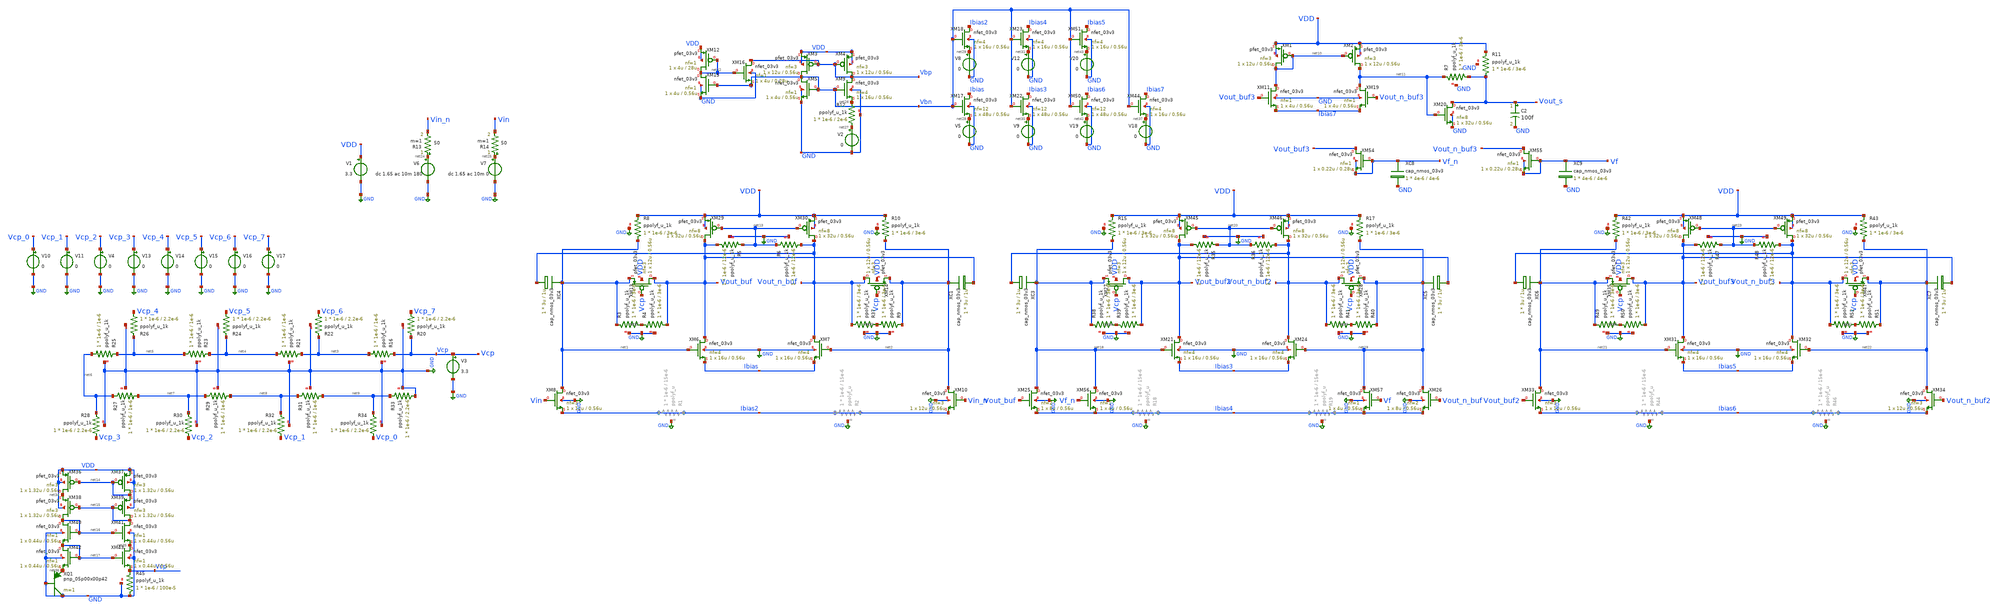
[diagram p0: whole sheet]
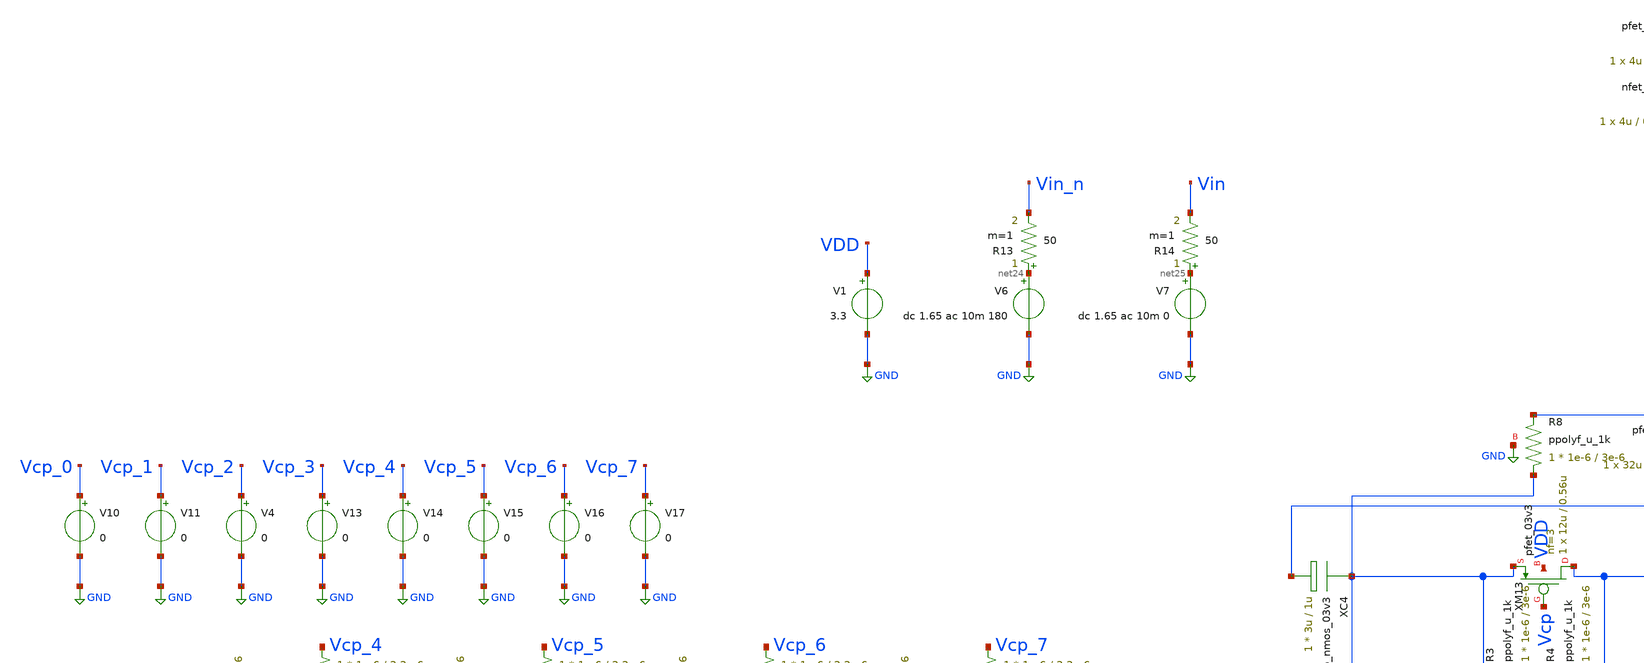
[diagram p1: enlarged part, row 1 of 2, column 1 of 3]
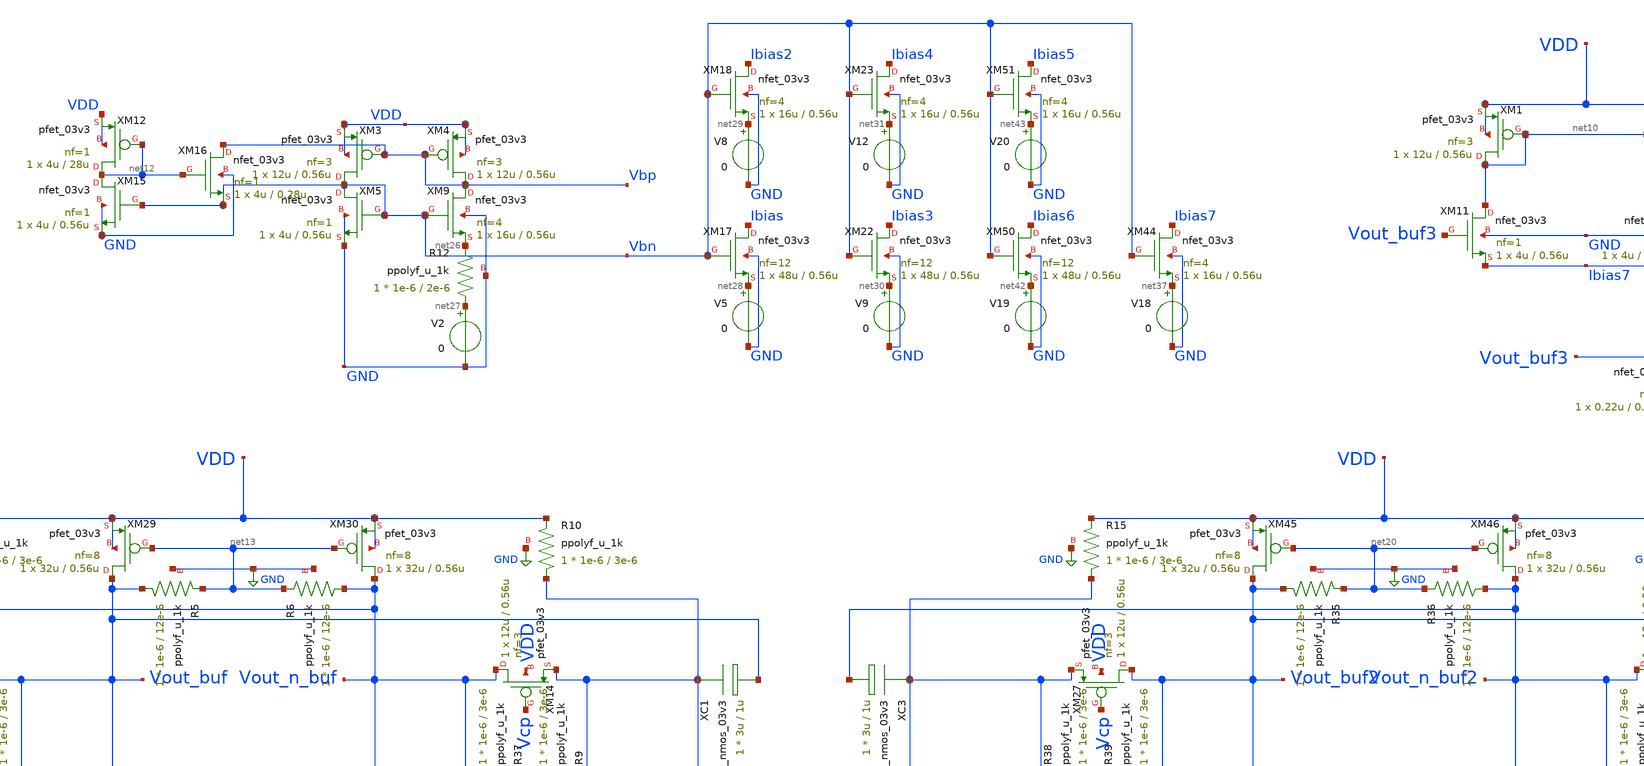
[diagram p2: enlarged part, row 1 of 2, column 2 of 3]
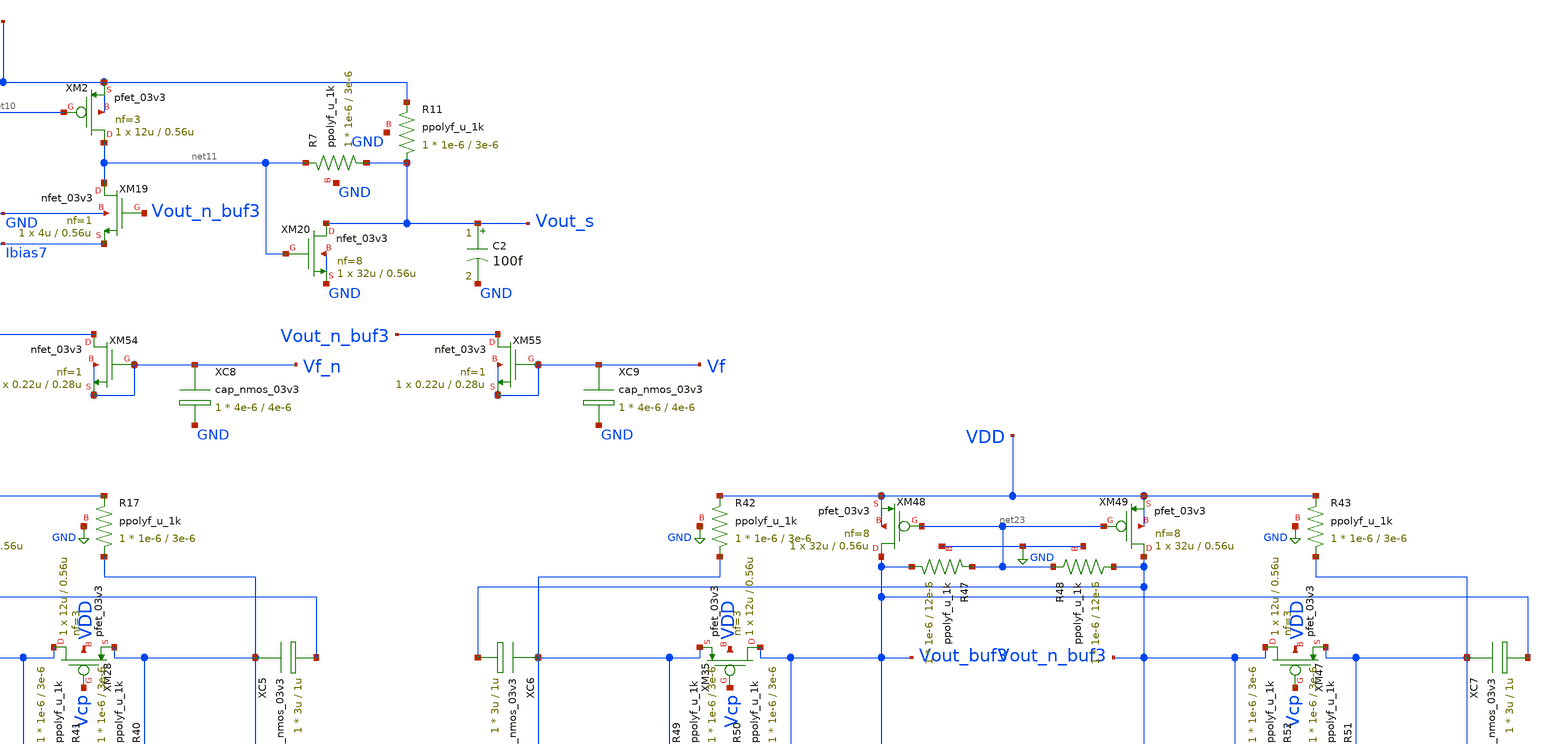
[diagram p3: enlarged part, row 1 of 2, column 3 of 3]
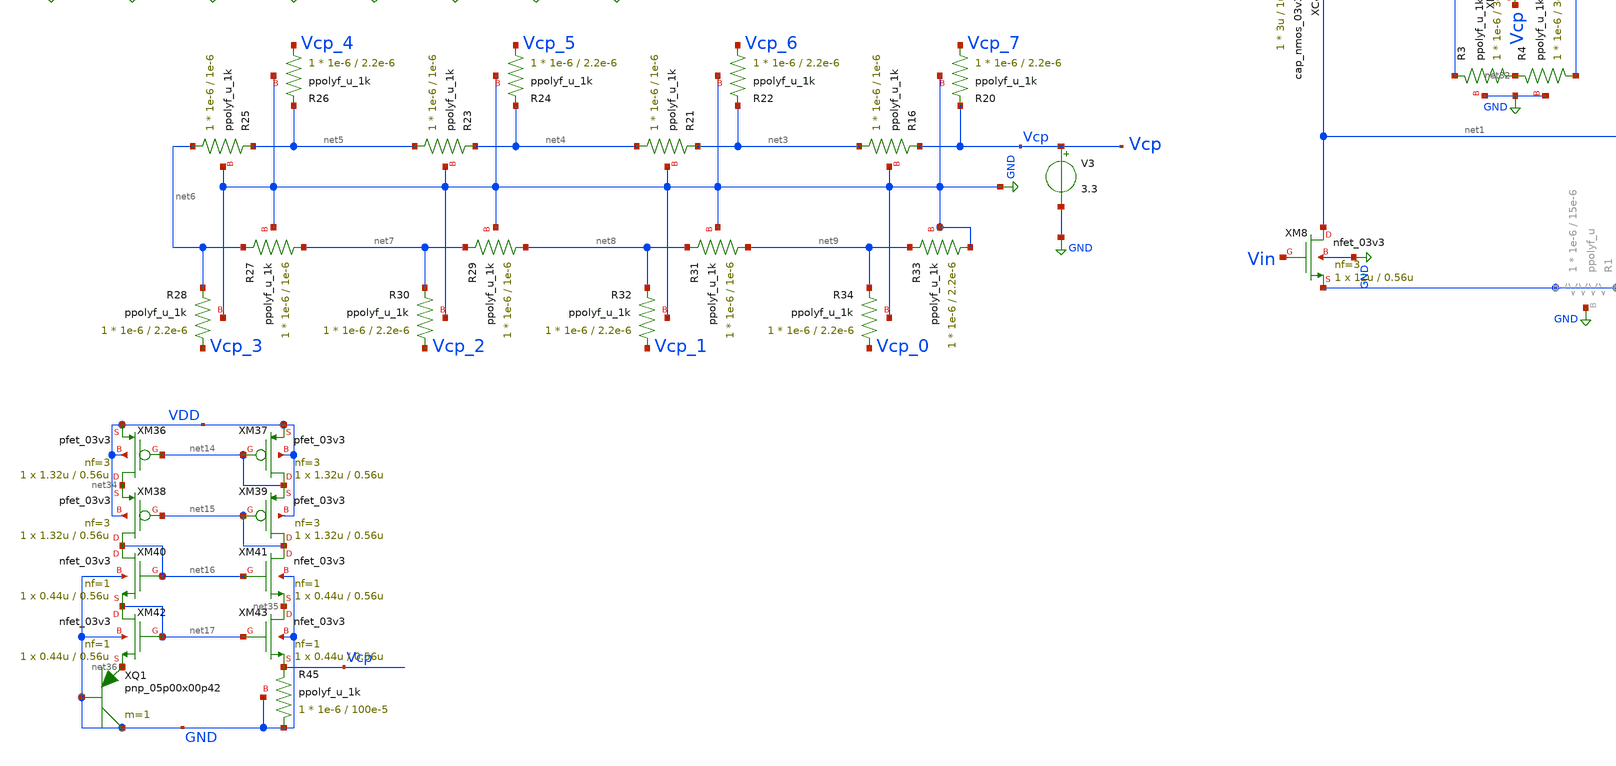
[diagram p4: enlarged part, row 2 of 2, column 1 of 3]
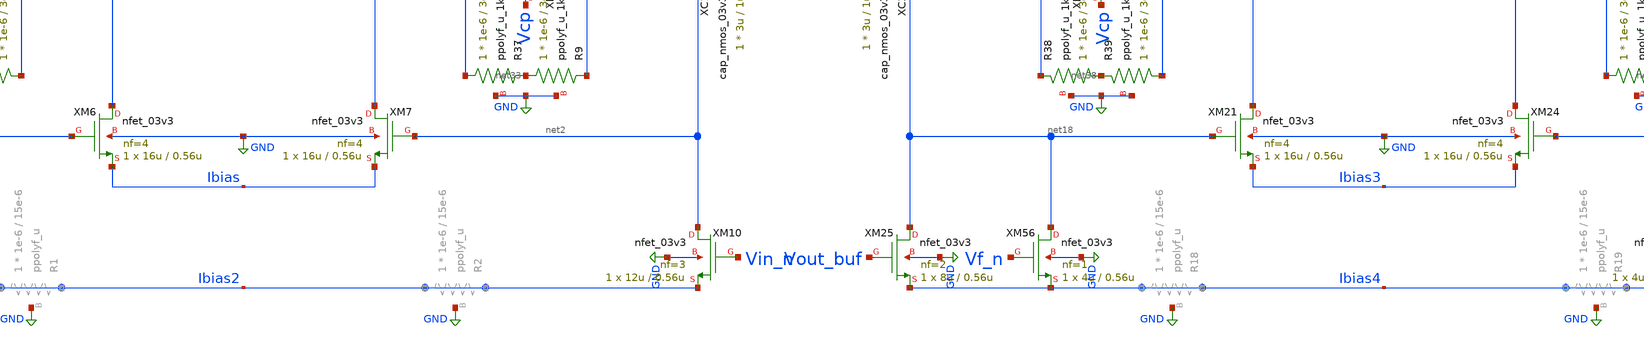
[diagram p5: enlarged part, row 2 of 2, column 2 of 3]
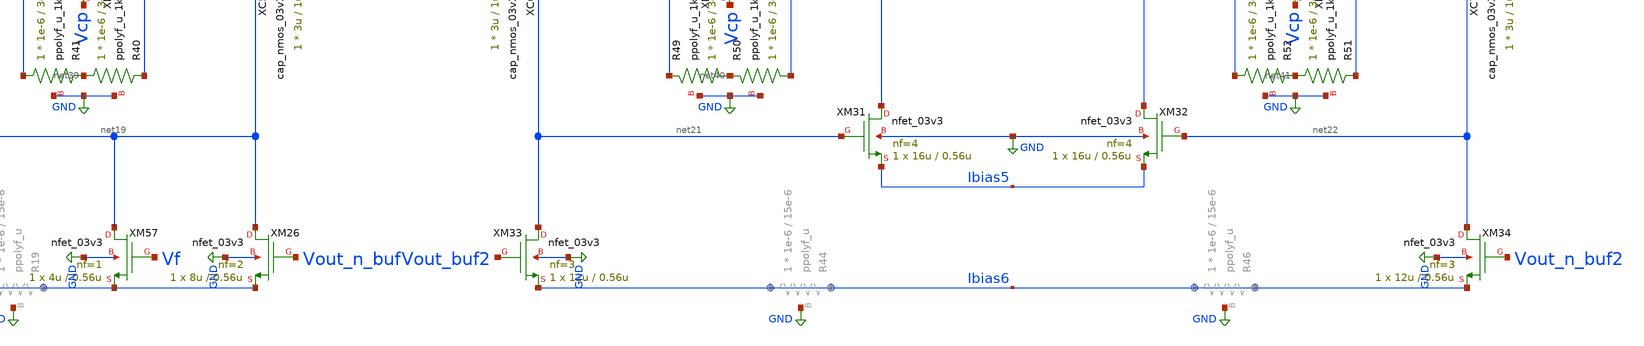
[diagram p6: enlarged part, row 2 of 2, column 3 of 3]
** sch_path: blocks/vga/vga.sch
**.subckt vga
V1 VDD GND 3.3
V6 net24 GND dc 1.65 ac 10m 180
XM6 Vout_buf net1 Ibias GND nfet_03v3 L=0.56u W=16u nf=4 ad='int((nf+1)/2) * W/nf * 0.18u' as='int((nf+2)/2) * W/nf * 0.18u'
+ pd='2*int((nf+1)/2) * (W/nf + 0.18u)' ps='2*int((nf+2)/2) * (W/nf + 0.18u)' nrd='0.18u / W' nrs='0.18u / W'
+ sa=0 sb=0 sd=0 m=1
XM7 Vout_n_buf net2 Ibias GND nfet_03v3 L=0.56u W=16u nf=4 ad='int((nf+1)/2) * W/nf * 0.18u' as='int((nf+2)/2) * W/nf * 0.18u'
+ pd='2*int((nf+1)/2) * (W/nf + 0.18u)' ps='2*int((nf+2)/2) * (W/nf + 0.18u)' nrd='0.18u / W' nrs='0.18u / W'
+ sa=0 sb=0 sd=0 m=1
XM8 net1 Vin Ibias2 GND nfet_03v3 L=0.56u W=12u nf=3 ad='int((nf+1)/2) * W/nf * 0.18u' as='int((nf+2)/2) * W/nf * 0.18u'
+ pd='2*int((nf+1)/2) * (W/nf + 0.18u)' ps='2*int((nf+2)/2) * (W/nf + 0.18u)' nrd='0.18u / W' nrs='0.18u / W'
+ sa=0 sb=0 sd=0 m=1
XM10 net2 Vin_n Ibias2 GND nfet_03v3 L=0.56u W=12u nf=3 ad='int((nf+1)/2) * W/nf * 0.18u' as='int((nf+2)/2) * W/nf * 0.18u'
+ pd='2*int((nf+1)/2) * (W/nf + 0.18u)' ps='2*int((nf+2)/2) * (W/nf + 0.18u)' nrd='0.18u / W' nrs='0.18u / W'
+ sa=0 sb=0 sd=0 m=1
V7 net25 GND dc 1.65 ac 10m 0
R14 net25 Vin 50 m=1
R13 net24 Vin_n 50 m=1
XR16 net3 Vcp GND ppolyf_u_1k r_width=1e-6 r_length=1e-6 m=1
XR20 Vcp_7 Vcp GND ppolyf_u_1k r_width=1e-6 r_length=2.2e-6 m=1
XR21 net4 net3 GND ppolyf_u_1k r_width=1e-6 r_length=1e-6 m=1
XR22 Vcp_6 net3 GND ppolyf_u_1k r_width=1e-6 r_length=2.2e-6 m=1
XR23 net5 net4 GND ppolyf_u_1k r_width=1e-6 r_length=1e-6 m=1
XR24 Vcp_5 net4 GND ppolyf_u_1k r_width=1e-6 r_length=2.2e-6 m=1
XR25 net6 net5 GND ppolyf_u_1k r_width=1e-6 r_length=1e-6 m=1
XR26 Vcp_4 net5 GND ppolyf_u_1k r_width=1e-6 r_length=2.2e-6 m=1
XR27 net7 net6 GND ppolyf_u_1k r_width=1e-6 r_length=1e-6 m=1
XR28 Vcp_3 net6 GND ppolyf_u_1k r_width=1e-6 r_length=2.2e-6 m=1
XR29 net8 net7 GND ppolyf_u_1k r_width=1e-6 r_length=1e-6 m=1
XR30 Vcp_2 net7 GND ppolyf_u_1k r_width=1e-6 r_length=2.2e-6 m=1
XR31 net9 net8 GND ppolyf_u_1k r_width=1e-6 r_length=1e-6 m=1
XR32 Vcp_1 net8 GND ppolyf_u_1k r_width=1e-6 r_length=2.2e-6 m=1
XR33 GND net9 GND ppolyf_u_1k r_width=1e-6 r_length=2.2e-6 m=1
XR34 Vcp_0 net9 GND ppolyf_u_1k r_width=1e-6 r_length=2.2e-6 m=1
V10 Vcp_0 GND 0
V11 Vcp_1 GND 0
V4 Vcp_2 GND 0
V13 Vcp_3 GND 0
V14 Vcp_4 GND 0
V15 Vcp_5 GND 0
V16 Vcp_6 GND 0
V17 Vcp_7 GND 0
V3 Vcp GND 3.3
XM13 Vout_buf Vcp net1 VDD pfet_03v3 L=0.56u W=12u nf=3 ad='int((nf+1)/2) * W/nf * 0.18u' as='int((nf+2)/2) * W/nf * 0.18u'
+ pd='2*int((nf+1)/2) * (W/nf + 0.18u)' ps='2*int((nf+2)/2) * (W/nf + 0.18u)' nrd='0.18u / W' nrs='0.18u / W'
+ sa=0 sb=0 sd=0 m=1
XM14 Vout_n_buf Vcp net2 VDD pfet_03v3 L=0.56u W=12u nf=3 ad='int((nf+1)/2) * W/nf * 0.18u' as='int((nf+2)/2) * W/nf * 0.18u'
+ pd='2*int((nf+1)/2) * (W/nf + 0.18u)' ps='2*int((nf+2)/2) * (W/nf + 0.18u)' nrd='0.18u / W' nrs='0.18u / W'
+ sa=0 sb=0 sd=0 m=1
XR8 net1 VDD GND ppolyf_u_1k r_width=1e-6 r_length=3e-6 m=1
XR10 net2 VDD GND ppolyf_u_1k r_width=1e-6 r_length=3e-6 m=1
XC4 net1 Vout_n_buf cap_nmos_03v3 c_width=3u c_length=1u m=1
XC1 net2 Vout_buf cap_nmos_03v3 c_width=3u c_length=1u m=1
XM11 net10 Vout_buf3 Ibias7 GND nfet_03v3 L=0.56u W=4u nf=1 ad='int((nf+1)/2) * W/nf * 0.18u' as='int((nf+2)/2) * W/nf * 0.18u'
+ pd='2*int((nf+1)/2) * (W/nf + 0.18u)' ps='2*int((nf+2)/2) * (W/nf + 0.18u)' nrd='0.18u / W' nrs='0.18u / W'
+ sa=0 sb=0 sd=0 m=1
XM19 net11 Vout_n_buf3 Ibias7 GND nfet_03v3 L=0.56u W=4u nf=1 ad='int((nf+1)/2) * W/nf * 0.18u' as='int((nf+2)/2) * W/nf * 0.18u'
+ pd='2*int((nf+1)/2) * (W/nf + 0.18u)' ps='2*int((nf+2)/2) * (W/nf + 0.18u)' nrd='0.18u / W' nrs='0.18u / W'
+ sa=0 sb=0 sd=0 m=1
XR7 Vout_s net11 GND ppolyf_u_1k r_width=1e-6 r_length=3e-6 m=1
XM20 Vout_s net11 GND GND nfet_03v3 L=0.56u W=32u nf=8 ad='int((nf+1)/2) * W/nf * 0.18u' as='int((nf+2)/2) * W/nf * 0.18u'
+ pd='2*int((nf+1)/2) * (W/nf + 0.18u)' ps='2*int((nf+2)/2) * (W/nf + 0.18u)' nrd='0.18u / W' nrs='0.18u / W'
+ sa=0 sb=0 sd=0 m=1
C2 Vout_s GND 100f m=1
XR11 Vout_s VDD GND ppolyf_u_1k r_width=1e-6 r_length=3e-6 m=1
XM1 net10 net10 VDD VDD pfet_03v3 L=0.56u W=12u nf=3 ad='int((nf+1)/2) * W/nf * 0.18u' as='int((nf+2)/2) * W/nf * 0.18u'
+ pd='2*int((nf+1)/2) * (W/nf + 0.18u)' ps='2*int((nf+2)/2) * (W/nf + 0.18u)' nrd='0.18u / W' nrs='0.18u / W'
+ sa=0 sb=0 sd=0 m=1
XM2 net11 net10 VDD VDD pfet_03v3 L=0.56u W=12u nf=3 ad='int((nf+1)/2) * W/nf * 0.18u' as='int((nf+2)/2) * W/nf * 0.18u'
+ pd='2*int((nf+1)/2) * (W/nf + 0.18u)' ps='2*int((nf+2)/2) * (W/nf + 0.18u)' nrd='0.18u / W' nrs='0.18u / W'
+ sa=0 sb=0 sd=0 m=1
XM3 Vbn Vbp VDD VDD pfet_03v3 L=0.56u W=12u nf=3 ad='int((nf+1)/2) * W/nf * 0.18u' as='int((nf+2)/2) * W/nf * 0.18u'
+ pd='2*int((nf+1)/2) * (W/nf + 0.18u)' ps='2*int((nf+2)/2) * (W/nf + 0.18u)' nrd='0.18u / W' nrs='0.18u / W'
+ sa=0 sb=0 sd=0 m=1
XM4 Vbp Vbp VDD VDD pfet_03v3 L=0.56u W=12u nf=3 ad='int((nf+1)/2) * W/nf * 0.18u' as='int((nf+2)/2) * W/nf * 0.18u'
+ pd='2*int((nf+1)/2) * (W/nf + 0.18u)' ps='2*int((nf+2)/2) * (W/nf + 0.18u)' nrd='0.18u / W' nrs='0.18u / W'
+ sa=0 sb=0 sd=0 m=1
XM5 Vbn Vbn GND GND nfet_03v3 L=0.56u W=4u nf=1 ad='int((nf+1)/2) * W/nf * 0.18u' as='int((nf+2)/2) * W/nf * 0.18u'
+ pd='2*int((nf+1)/2) * (W/nf + 0.18u)' ps='2*int((nf+2)/2) * (W/nf + 0.18u)' nrd='0.18u / W' nrs='0.18u / W'
+ sa=0 sb=0 sd=0 m=1
XM9 Vbp Vbn net26 GND nfet_03v3 L=0.56u W=16u nf=4 ad='int((nf+1)/2) * W/nf * 0.18u' as='int((nf+2)/2) * W/nf * 0.18u'
+ pd='2*int((nf+1)/2) * (W/nf + 0.18u)' ps='2*int((nf+2)/2) * (W/nf + 0.18u)' nrd='0.18u / W' nrs='0.18u / W'
+ sa=0 sb=0 sd=0 m=1
XM12 net12 net12 VDD VDD pfet_03v3 L=28u W=4u nf=1 ad='int((nf+1)/2) * W/nf * 0.18u' as='int((nf+2)/2) * W/nf * 0.18u'
+ pd='2*int((nf+1)/2) * (W/nf + 0.18u)' ps='2*int((nf+2)/2) * (W/nf + 0.18u)' nrd='0.18u / W' nrs='0.18u / W'
+ sa=0 sb=0 sd=0 m=1
XM15 net12 Vbn GND GND nfet_03v3 L=0.56u W=4u nf=1 ad='int((nf+1)/2) * W/nf * 0.18u' as='int((nf+2)/2) * W/nf * 0.18u'
+ pd='2*int((nf+1)/2) * (W/nf + 0.18u)' ps='2*int((nf+2)/2) * (W/nf + 0.18u)' nrd='0.18u / W' nrs='0.18u / W'
+ sa=0 sb=0 sd=0 m=1
XM16 Vbp net12 Vbn GND nfet_03v3 L=0.28u W=4u nf=1 ad='int((nf+1)/2) * W/nf * 0.18u' as='int((nf+2)/2) * W/nf * 0.18u'
+ pd='2*int((nf+1)/2) * (W/nf + 0.18u)' ps='2*int((nf+2)/2) * (W/nf + 0.18u)' nrd='0.18u / W' nrs='0.18u / W'
+ sa=0 sb=0 sd=0 m=1
XR12 net27 net26 GND ppolyf_u_1k r_width=1e-6 r_length=2e-6 m=1
V2 net27 GND 0
XM17 Ibias Vbn net28 GND nfet_03v3 L=0.56u W=48u nf=12 ad='int((nf+1)/2) * W/nf * 0.18u' as='int((nf+2)/2) * W/nf * 0.18u'
+ pd='2*int((nf+1)/2) * (W/nf + 0.18u)' ps='2*int((nf+2)/2) * (W/nf + 0.18u)' nrd='0.18u / W' nrs='0.18u / W'
+ sa=0 sb=0 sd=0 m=1
V5 net28 GND 0
XM18 Ibias2 Vbn net29 GND nfet_03v3 L=0.56u W=16u nf=4 ad='int((nf+1)/2) * W/nf * 0.18u' as='int((nf+2)/2) * W/nf * 0.18u'
+ pd='2*int((nf+1)/2) * (W/nf + 0.18u)' ps='2*int((nf+2)/2) * (W/nf + 0.18u)' nrd='0.18u / W' nrs='0.18u / W'
+ sa=0 sb=0 sd=0 m=1
V8 net29 GND 0
XM22 Ibias3 Vbn net30 GND nfet_03v3 L=0.56u W=48u nf=12 ad='int((nf+1)/2) * W/nf * 0.18u' as='int((nf+2)/2) * W/nf * 0.18u'
+ pd='2*int((nf+1)/2) * (W/nf + 0.18u)' ps='2*int((nf+2)/2) * (W/nf + 0.18u)' nrd='0.18u / W' nrs='0.18u / W'
+ sa=0 sb=0 sd=0 m=1
V9 net30 GND 0
XM23 Ibias4 Vbn net31 GND nfet_03v3 L=0.56u W=16u nf=4 ad='int((nf+1)/2) * W/nf * 0.18u' as='int((nf+2)/2) * W/nf * 0.18u'
+ pd='2*int((nf+1)/2) * (W/nf + 0.18u)' ps='2*int((nf+2)/2) * (W/nf + 0.18u)' nrd='0.18u / W' nrs='0.18u / W'
+ sa=0 sb=0 sd=0 m=1
V12 net31 GND 0
XM29 Vout_buf net13 VDD VDD pfet_03v3 L=0.56u W=32u nf=8 ad='int((nf+1)/2) * W/nf * 0.18u' as='int((nf+2)/2) * W/nf * 0.18u'
+ pd='2*int((nf+1)/2) * (W/nf + 0.18u)' ps='2*int((nf+2)/2) * (W/nf + 0.18u)' nrd='0.18u / W' nrs='0.18u / W'
+ sa=0 sb=0 sd=0 m=1
XM30 Vout_n_buf net13 VDD VDD pfet_03v3 L=0.56u W=32u nf=8 ad='int((nf+1)/2) * W/nf * 0.18u' as='int((nf+2)/2) * W/nf * 0.18u'
+ pd='2*int((nf+1)/2) * (W/nf + 0.18u)' ps='2*int((nf+2)/2) * (W/nf + 0.18u)' nrd='0.18u / W' nrs='0.18u / W'
+ sa=0 sb=0 sd=0 m=1
XR5 Vout_buf net13 GND ppolyf_u_1k r_width=1e-6 r_length=12e-6 m=1
XR6 Vout_n_buf net13 GND ppolyf_u_1k r_width=1e-6 r_length=12e-6 m=1
XR3 net32 net1 GND ppolyf_u_1k r_width=1e-6 r_length=3e-6 m=1
XR4 Vout_buf net32 GND ppolyf_u_1k r_width=1e-6 r_length=3e-6 m=1
XR9 net33 net2 GND ppolyf_u_1k r_width=1e-6 r_length=3e-6 m=1
XR37 Vout_n_buf net33 GND ppolyf_u_1k r_width=1e-6 r_length=3e-6 m=1
XM36 net34 net14 VDD VDD pfet_03v3 L=0.56u W=1.32u nf=3 ad='int((nf+1)/2) * W/nf * 0.18u' as='int((nf+2)/2) * W/nf * 0.18u'
+ pd='2*int((nf+1)/2) * (W/nf + 0.18u)' ps='2*int((nf+2)/2) * (W/nf + 0.18u)' nrd='0.18u / W' nrs='0.18u / W'
+ sa=0 sb=0 sd=0 m=1
XM37 net14 net14 VDD VDD pfet_03v3 L=0.56u W=1.32u nf=3 ad='int((nf+1)/2) * W/nf * 0.18u' as='int((nf+2)/2) * W/nf * 0.18u'
+ pd='2*int((nf+1)/2) * (W/nf + 0.18u)' ps='2*int((nf+2)/2) * (W/nf + 0.18u)' nrd='0.18u / W' nrs='0.18u / W'
+ sa=0 sb=0 sd=0 m=1
XM38 net16 net15 net34 VDD pfet_03v3 L=0.56u W=1.32u nf=3 ad='int((nf+1)/2) * W/nf * 0.18u' as='int((nf+2)/2) * W/nf * 0.18u'
+ pd='2*int((nf+1)/2) * (W/nf + 0.18u)' ps='2*int((nf+2)/2) * (W/nf + 0.18u)' nrd='0.18u / W' nrs='0.18u / W'
+ sa=0 sb=0 sd=0 m=1
XM39 net15 net15 net14 VDD pfet_03v3 L=0.56u W=1.32u nf=3 ad='int((nf+1)/2) * W/nf * 0.18u' as='int((nf+2)/2) * W/nf * 0.18u'
+ pd='2*int((nf+1)/2) * (W/nf + 0.18u)' ps='2*int((nf+2)/2) * (W/nf + 0.18u)' nrd='0.18u / W' nrs='0.18u / W'
+ sa=0 sb=0 sd=0 m=1
XM40 net16 net16 net17 GND nfet_03v3 L=0.56u W=0.44u nf=1 ad='int((nf+1)/2) * W/nf * 0.18u' as='int((nf+2)/2) * W/nf * 0.18u'
+ pd='2*int((nf+1)/2) * (W/nf + 0.18u)' ps='2*int((nf+2)/2) * (W/nf + 0.18u)' nrd='0.18u / W' nrs='0.18u / W'
+ sa=0 sb=0 sd=0 m=1
XM41 net15 net16 net35 GND nfet_03v3 L=0.56u W=0.44u nf=1 ad='int((nf+1)/2) * W/nf * 0.18u' as='int((nf+2)/2) * W/nf * 0.18u'
+ pd='2*int((nf+1)/2) * (W/nf + 0.18u)' ps='2*int((nf+2)/2) * (W/nf + 0.18u)' nrd='0.18u / W' nrs='0.18u / W'
+ sa=0 sb=0 sd=0 m=1
XM42 net17 net17 net36 GND nfet_03v3 L=0.56u W=0.44u nf=1 ad='int((nf+1)/2) * W/nf * 0.18u' as='int((nf+2)/2) * W/nf * 0.18u'
+ pd='2*int((nf+1)/2) * (W/nf + 0.18u)' ps='2*int((nf+2)/2) * (W/nf + 0.18u)' nrd='0.18u / W' nrs='0.18u / W'
+ sa=0 sb=0 sd=0 m=1
XM43 net35 net17 Vcp GND nfet_03v3 L=0.56u W=0.44u nf=1 ad='int((nf+1)/2) * W/nf * 0.18u' as='int((nf+2)/2) * W/nf * 0.18u'
+ pd='2*int((nf+1)/2) * (W/nf + 0.18u)' ps='2*int((nf+2)/2) * (W/nf + 0.18u)' nrd='0.18u / W' nrs='0.18u / W'
+ sa=0 sb=0 sd=0 m=1
XQ1 GND GND net36 pnp_05p00x00p42 m=1 par=1
XR45 GND Vcp GND ppolyf_u_1k r_width=1e-6 r_length=100e-5 m=1
XM44 Ibias7 Vbn net37 GND nfet_03v3 L=0.56u W=16u nf=4 ad='int((nf+1)/2) * W/nf * 0.18u' as='int((nf+2)/2) * W/nf * 0.18u'
+ pd='2*int((nf+1)/2) * (W/nf + 0.18u)' ps='2*int((nf+2)/2) * (W/nf + 0.18u)' nrd='0.18u / W' nrs='0.18u / W'
+ sa=0 sb=0 sd=0 m=1
V18 net37 GND 0
XM21 Vout_buf2 net18 Ibias3 GND nfet_03v3 L=0.56u W=16u nf=4 ad='int((nf+1)/2) * W/nf * 0.18u' as='int((nf+2)/2) * W/nf * 0.18u'
+ pd='2*int((nf+1)/2) * (W/nf + 0.18u)' ps='2*int((nf+2)/2) * (W/nf + 0.18u)' nrd='0.18u / W' nrs='0.18u / W'
+ sa=0 sb=0 sd=0 m=1
XM24 Vout_n_buf2 net19 Ibias3 GND nfet_03v3 L=0.56u W=16u nf=4 ad='int((nf+1)/2) * W/nf * 0.18u' as='int((nf+2)/2) * W/nf * 0.18u'
+ pd='2*int((nf+1)/2) * (W/nf + 0.18u)' ps='2*int((nf+2)/2) * (W/nf + 0.18u)' nrd='0.18u / W' nrs='0.18u / W'
+ sa=0 sb=0 sd=0 m=1
XM25 net18 Vout_buf Ibias4 GND nfet_03v3 L=0.56u W=8u nf=2 ad='int((nf+1)/2) * W/nf * 0.18u' as='int((nf+2)/2) * W/nf * 0.18u'
+ pd='2*int((nf+1)/2) * (W/nf + 0.18u)' ps='2*int((nf+2)/2) * (W/nf + 0.18u)' nrd='0.18u / W' nrs='0.18u / W'
+ sa=0 sb=0 sd=0 m=1
XM26 net19 Vout_n_buf Ibias4 GND nfet_03v3 L=0.56u W=8u nf=2 ad='int((nf+1)/2) * W/nf * 0.18u' as='int((nf+2)/2) * W/nf * 0.18u'
+ pd='2*int((nf+1)/2) * (W/nf + 0.18u)' ps='2*int((nf+2)/2) * (W/nf + 0.18u)' nrd='0.18u / W' nrs='0.18u / W'
+ sa=0 sb=0 sd=0 m=1
XM27 Vout_buf2 Vcp net18 VDD pfet_03v3 L=0.56u W=12u nf=3 ad='int((nf+1)/2) * W/nf * 0.18u' as='int((nf+2)/2) * W/nf * 0.18u'
+ pd='2*int((nf+1)/2) * (W/nf + 0.18u)' ps='2*int((nf+2)/2) * (W/nf + 0.18u)' nrd='0.18u / W' nrs='0.18u / W'
+ sa=0 sb=0 sd=0 m=1
XM28 Vout_n_buf2 Vcp net19 VDD pfet_03v3 L=0.56u W=12u nf=3 ad='int((nf+1)/2) * W/nf * 0.18u' as='int((nf+2)/2) * W/nf * 0.18u'
+ pd='2*int((nf+1)/2) * (W/nf + 0.18u)' ps='2*int((nf+2)/2) * (W/nf + 0.18u)' nrd='0.18u / W' nrs='0.18u / W'
+ sa=0 sb=0 sd=0 m=1
XR15 net18 VDD GND ppolyf_u_1k r_width=1e-6 r_length=3e-6 m=1
XR17 net19 VDD GND ppolyf_u_1k r_width=1e-6 r_length=3e-6 m=1
XC3 net18 Vout_n_buf2 cap_nmos_03v3 c_width=3u c_length=1u m=1
XC5 net19 Vout_buf2 cap_nmos_03v3 c_width=3u c_length=1u m=1
XM45 Vout_buf2 net20 VDD VDD pfet_03v3 L=0.56u W=32u nf=8 ad='int((nf+1)/2) * W/nf * 0.18u' as='int((nf+2)/2) * W/nf * 0.18u'
+ pd='2*int((nf+1)/2) * (W/nf + 0.18u)' ps='2*int((nf+2)/2) * (W/nf + 0.18u)' nrd='0.18u / W' nrs='0.18u / W'
+ sa=0 sb=0 sd=0 m=1
XM46 Vout_n_buf2 net20 VDD VDD pfet_03v3 L=0.56u W=32u nf=8 ad='int((nf+1)/2) * W/nf * 0.18u' as='int((nf+2)/2) * W/nf * 0.18u'
+ pd='2*int((nf+1)/2) * (W/nf + 0.18u)' ps='2*int((nf+2)/2) * (W/nf + 0.18u)' nrd='0.18u / W' nrs='0.18u / W'
+ sa=0 sb=0 sd=0 m=1
XR35 Vout_buf2 net20 GND ppolyf_u_1k r_width=1e-6 r_length=12e-6 m=1
XR36 Vout_n_buf2 net20 GND ppolyf_u_1k r_width=1e-6 r_length=12e-6 m=1
XR38 net38 net18 GND ppolyf_u_1k r_width=1e-6 r_length=3e-6 m=1
XR39 Vout_buf2 net38 GND ppolyf_u_1k r_width=1e-6 r_length=3e-6 m=1
XR40 net39 net19 GND ppolyf_u_1k r_width=1e-6 r_length=3e-6 m=1
XR41 Vout_n_buf2 net39 GND ppolyf_u_1k r_width=1e-6 r_length=3e-6 m=1
XM31 Vout_buf3 net21 Ibias5 GND nfet_03v3 L=0.56u W=16u nf=4 ad='int((nf+1)/2) * W/nf * 0.18u' as='int((nf+2)/2) * W/nf * 0.18u'
+ pd='2*int((nf+1)/2) * (W/nf + 0.18u)' ps='2*int((nf+2)/2) * (W/nf + 0.18u)' nrd='0.18u / W' nrs='0.18u / W'
+ sa=0 sb=0 sd=0 m=1
XM32 Vout_n_buf3 net22 Ibias5 GND nfet_03v3 L=0.56u W=16u nf=4 ad='int((nf+1)/2) * W/nf * 0.18u' as='int((nf+2)/2) * W/nf * 0.18u'
+ pd='2*int((nf+1)/2) * (W/nf + 0.18u)' ps='2*int((nf+2)/2) * (W/nf + 0.18u)' nrd='0.18u / W' nrs='0.18u / W'
+ sa=0 sb=0 sd=0 m=1
XM33 net21 Vout_buf2 Ibias6 GND nfet_03v3 L=0.56u W=12u nf=3 ad='int((nf+1)/2) * W/nf * 0.18u' as='int((nf+2)/2) * W/nf * 0.18u'
+ pd='2*int((nf+1)/2) * (W/nf + 0.18u)' ps='2*int((nf+2)/2) * (W/nf + 0.18u)' nrd='0.18u / W' nrs='0.18u / W'
+ sa=0 sb=0 sd=0 m=1
XM34 net22 Vout_n_buf2 Ibias6 GND nfet_03v3 L=0.56u W=12u nf=3 ad='int((nf+1)/2) * W/nf * 0.18u' as='int((nf+2)/2) * W/nf * 0.18u'
+ pd='2*int((nf+1)/2) * (W/nf + 0.18u)' ps='2*int((nf+2)/2) * (W/nf + 0.18u)' nrd='0.18u / W' nrs='0.18u / W'
+ sa=0 sb=0 sd=0 m=1
XM35 Vout_buf3 Vcp net21 VDD pfet_03v3 L=0.56u W=12u nf=3 ad='int((nf+1)/2) * W/nf * 0.18u' as='int((nf+2)/2) * W/nf * 0.18u'
+ pd='2*int((nf+1)/2) * (W/nf + 0.18u)' ps='2*int((nf+2)/2) * (W/nf + 0.18u)' nrd='0.18u / W' nrs='0.18u / W'
+ sa=0 sb=0 sd=0 m=1
XM47 Vout_n_buf3 Vcp net22 VDD pfet_03v3 L=0.56u W=12u nf=3 ad='int((nf+1)/2) * W/nf * 0.18u' as='int((nf+2)/2) * W/nf * 0.18u'
+ pd='2*int((nf+1)/2) * (W/nf + 0.18u)' ps='2*int((nf+2)/2) * (W/nf + 0.18u)' nrd='0.18u / W' nrs='0.18u / W'
+ sa=0 sb=0 sd=0 m=1
XR42 net21 VDD GND ppolyf_u_1k r_width=1e-6 r_length=3e-6 m=1
XR43 net22 VDD GND ppolyf_u_1k r_width=1e-6 r_length=3e-6 m=1
XC6 net21 Vout_n_buf3 cap_nmos_03v3 c_width=3u c_length=1u m=1
XC7 net22 Vout_buf3 cap_nmos_03v3 c_width=3u c_length=1u m=1
XM48 Vout_buf3 net23 VDD VDD pfet_03v3 L=0.56u W=32u nf=8 ad='int((nf+1)/2) * W/nf * 0.18u' as='int((nf+2)/2) * W/nf * 0.18u'
+ pd='2*int((nf+1)/2) * (W/nf + 0.18u)' ps='2*int((nf+2)/2) * (W/nf + 0.18u)' nrd='0.18u / W' nrs='0.18u / W'
+ sa=0 sb=0 sd=0 m=1
XM49 Vout_n_buf3 net23 VDD VDD pfet_03v3 L=0.56u W=32u nf=8 ad='int((nf+1)/2) * W/nf * 0.18u' as='int((nf+2)/2) * W/nf * 0.18u'
+ pd='2*int((nf+1)/2) * (W/nf + 0.18u)' ps='2*int((nf+2)/2) * (W/nf + 0.18u)' nrd='0.18u / W' nrs='0.18u / W'
+ sa=0 sb=0 sd=0 m=1
XR47 Vout_buf3 net23 GND ppolyf_u_1k r_width=1e-6 r_length=12e-6 m=1
XR48 Vout_n_buf3 net23 GND ppolyf_u_1k r_width=1e-6 r_length=12e-6 m=1
XR49 net40 net21 GND ppolyf_u_1k r_width=1e-6 r_length=3e-6 m=1
XR50 Vout_buf3 net40 GND ppolyf_u_1k r_width=1e-6 r_length=3e-6 m=1
XR51 net41 net22 GND ppolyf_u_1k r_width=1e-6 r_length=3e-6 m=1
XR52 Vout_n_buf3 net41 GND ppolyf_u_1k r_width=1e-6 r_length=3e-6 m=1
XM50 Ibias6 Vbn net42 GND nfet_03v3 L=0.56u W=48u nf=12 ad='int((nf+1)/2) * W/nf * 0.18u' as='int((nf+2)/2) * W/nf * 0.18u'
+ pd='2*int((nf+1)/2) * (W/nf + 0.18u)' ps='2*int((nf+2)/2) * (W/nf + 0.18u)' nrd='0.18u / W' nrs='0.18u / W'
+ sa=0 sb=0 sd=0 m=1
V19 net42 GND 0
XM51 Ibias5 Vbn net43 GND nfet_03v3 L=0.56u W=16u nf=4 ad='int((nf+1)/2) * W/nf * 0.18u' as='int((nf+2)/2) * W/nf * 0.18u'
+ pd='2*int((nf+1)/2) * (W/nf + 0.18u)' ps='2*int((nf+2)/2) * (W/nf + 0.18u)' nrd='0.18u / W' nrs='0.18u / W'
+ sa=0 sb=0 sd=0 m=1
V20 net43 GND 0
XM54 Vout_buf3 Vf_n Vf_n Vf_n nfet_03v3 L=0.28u W=0.22u nf=1 ad='int((nf+1)/2) * W/nf * 0.18u' as='int((nf+2)/2) * W/nf * 0.18u'
+ pd='2*int((nf+1)/2) * (W/nf + 0.18u)' ps='2*int((nf+2)/2) * (W/nf + 0.18u)' nrd='0.18u / W' nrs='0.18u / W'
+ sa=0 sb=0 sd=0 m=1
XM55 Vout_n_buf3 Vf Vf Vf nfet_03v3 L=0.28u W=0.22u nf=1 ad='int((nf+1)/2) * W/nf * 0.18u' as='int((nf+2)/2) * W/nf * 0.18u'
+ pd='2*int((nf+1)/2) * (W/nf + 0.18u)' ps='2*int((nf+2)/2) * (W/nf + 0.18u)' nrd='0.18u / W' nrs='0.18u / W'
+ sa=0 sb=0 sd=0 m=1
XM56 net18 Vf_n Ibias4 GND nfet_03v3 L=0.56u W=4u nf=1 ad='int((nf+1)/2) * W/nf * 0.18u' as='int((nf+2)/2) * W/nf * 0.18u'
+ pd='2*int((nf+1)/2) * (W/nf + 0.18u)' ps='2*int((nf+2)/2) * (W/nf + 0.18u)' nrd='0.18u / W' nrs='0.18u / W'
+ sa=0 sb=0 sd=0 m=1
XM57 net19 Vf Ibias4 GND nfet_03v3 L=0.56u W=4u nf=1 ad='int((nf+1)/2) * W/nf * 0.18u' as='int((nf+2)/2) * W/nf * 0.18u'
+ pd='2*int((nf+1)/2) * (W/nf + 0.18u)' ps='2*int((nf+2)/2) * (W/nf + 0.18u)' nrd='0.18u / W' nrs='0.18u / W'
+ sa=0 sb=0 sd=0 m=1
XC8 Vf_n GND cap_nmos_03v3 c_width=4e-6 c_length=4e-6 m=1
XC9 Vf GND cap_nmos_03v3 c_width=4e-6 c_length=4e-6 m=1
**** begin user architecture code


.include /foss/pdks/gf180mcuD/libs.tech/ngspice/design.ngspice
.lib /foss/pdks/gf180mcuD/libs.tech/ngspice/sm141064.ngspice typical
.lib /foss/pdks/gf180mcuD/libs.tech/ngspice/sm141064.ngspice bjt_typical
.lib /foss/pdks/gf180mcuD/libs.tech/ngspice/sm141064.ngspice diode_typical
.lib /foss/pdks/gf180mcuD/libs.tech/ngspice/sm141064.ngspice res_typical
.lib /foss/pdks/gf180mcuD/libs.tech/ngspice/sm141064.ngspice mimcap_typical
.lib /foss/pdks/gf180mcuD/libs.tech/ngspice/sm141064.ngspice moscap_typical
.option method=gear

.control
set temp = 85

* this one is for conducting instantaneous power vs. time (transient analysis)
let freq = 1200meg
let pers = 100
let steps = 2000

let tper = 1 / freq
let tfin = pers * tper
let tstep = tfin / steps

let amp = 10m
let plotst = tfin - 2 * tper
let postamp = 5 * amp

alter @v6[sin] = [ 1.65 $&amp $&freq 0 0 0 ]
alter @v7[sin] = [ 1.65 $&amp $&freq 0 0 180 ]

* alter @v4[sin] = [ 1.65 $&postamp $&freq 0 0 0 ]
* alter @v8[sin] = [ 1.65 $&postamp $&freq 0 0 180 ]

tran $&tstep $&tfin
plot v(vout_s) v(vout_buf) v(vout_n_buf) v(vout_buf2) v(vout_n_buf2) v(vout_buf3) v(vout_n_buf3)
+ v(vin) v(vin_n) xlimit $&plotst $&tfin ylimit 1.4 2.4
* plot v(vf) v(vf_n) v(vbb) v(vbb2)

* let abc = v(vout_s)
* plot abc v(net9) v(net14) xlimit $&plotst $&tfin

let pwr = -1 * v1#branch * vdd
plot pwr ylimit 0 60m

print mean(v5#branch)
.endc


**** end user architecture code
**.ends
.GLOBAL GND
.end
